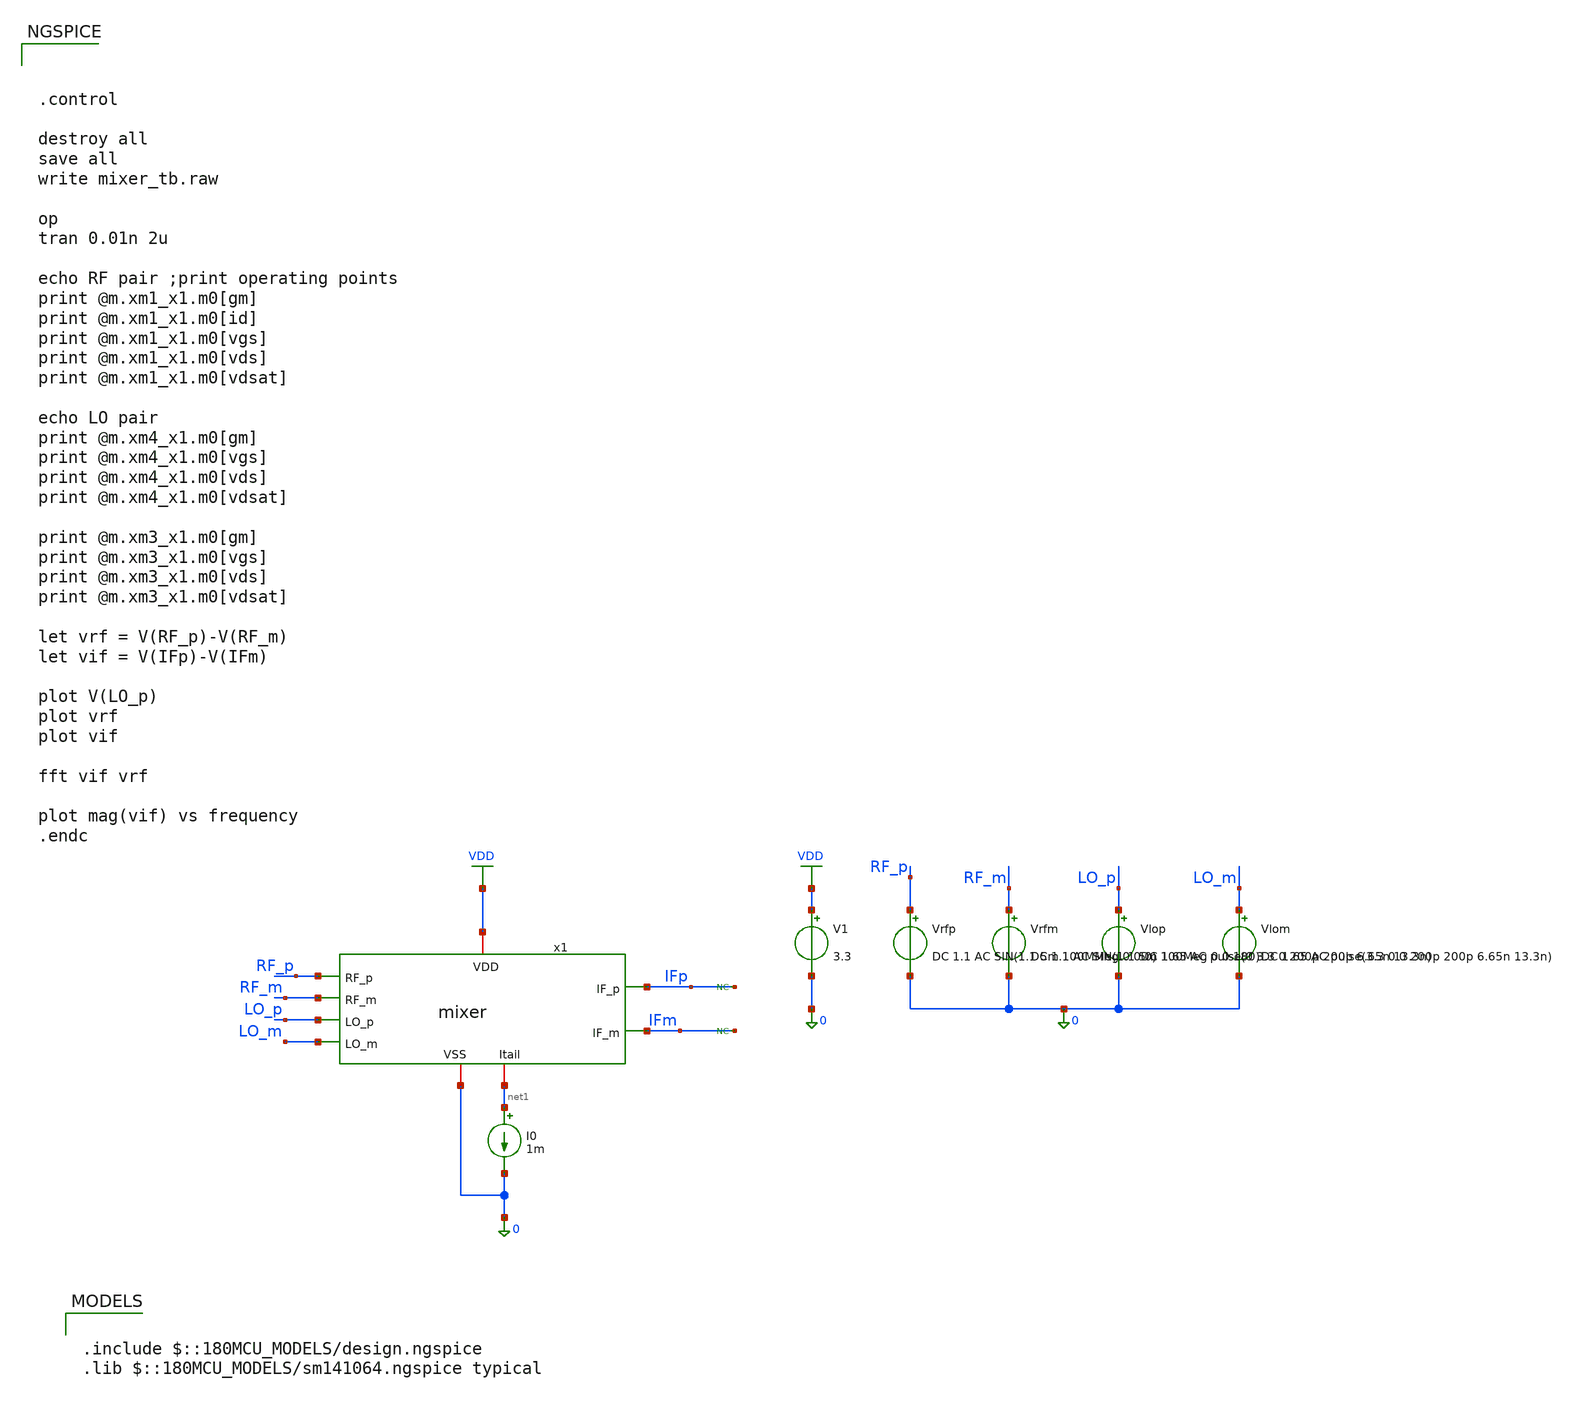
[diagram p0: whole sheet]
** sch_path: designs/mixer/testbench/mixer_tb.sch
**.subckt mixer_tb
V1 VDD 0 3.3
Vrfp RF_p 0 DC 1.1 AC SIN(1.1 5m 100MMeg 0 0 0)
Vrfm RF_m 0 DC 1.1 AC SIN(1.1 5m 100Meg 0 0 180)
I0 net1 0 1m
Vlop LO_p 0 DC 1.65 AC pulse(0 3.3 0 200p 200p 6.65n 13.3n)
Vlom LO_m 0 DC 1.65 AC pulse(3.3 0 0 200p 200p 6.65n 13.3n)
* noconn IFp
* noconn IFm
x1 IFp RF_p VDD 0 IFm RF_m LO_p net1 LO_m mixer
**** begin user architecture code

.include $::180MCU_MODELS/design.ngspice
.lib $::180MCU_MODELS/sm141064.ngspice typical




.control

destroy all
save all
write mixer_tb.raw

op
tran 0.01n 2u

echo RF pair ;print operating points
print @m.xm1_x1.m0[gm]
print @m.xm1_x1.m0[id]
print @m.xm1_x1.m0[vgs]
print @m.xm1_x1.m0[vds]
print @m.xm1_x1.m0[vdsat]

echo LO pair
print @m.xm4_x1.m0[gm]
print @m.xm4_x1.m0[vgs]
print @m.xm4_x1.m0[vds]
print @m.xm4_x1.m0[vdsat]

print @m.xm3_x1.m0[gm]
print @m.xm3_x1.m0[vgs]
print @m.xm3_x1.m0[vds]
print @m.xm3_x1.m0[vdsat]

let vrf = V(RF_p)-V(RF_m)
let vif = V(IFp)-V(IFm)

plot V(LO_p)
plot vrf
plot vif

fft vif vrf

plot mag(vif) vs frequency
.endc


**** end user architecture code
**.ends

* expanding   symbol:  /foss/designs/NYCMOS/designs/mixer/schematic/mixer.sym # of pins=9
** sym_path: designs/mixer/schematic/mixer.sym
** sch_path: designs/mixer/schematic/mixer.sch
.subckt mixer IF_p RF_p VDD VSS IF_m RF_m LO_p Itail LO_m
*.iopin VDD
*.ipin LO_p
*.ipin LO_m
*.iopin Itail
*.opin IF_m
*.opin IF_p
*.iopin VSS
*.ipin RF_p
*.ipin RF_m
XM1 net1 RF_p Itail VSS nfet_03v3 L=0.28u W=36u nf=6 ad='int((nf+1)/2) * W/nf * 0.18u' as='int((nf+2)/2) * W/nf * 0.18u'
+ pd='2*int((nf+1)/2) * (W/nf + 0.18u)' ps='2*int((nf+2)/2) * (W/nf + 0.18u)' nrd='0.18u / W' nrs='0.18u / W'
+ sa=0 sb=0 sd=0 m=1
XM2 net2 RF_m Itail VSS nfet_03v3 L=0.28u W=36u nf=6 ad='int((nf+1)/2) * W/nf * 0.18u' as='int((nf+2)/2) * W/nf * 0.18u'
+ pd='2*int((nf+1)/2) * (W/nf + 0.18u)' ps='2*int((nf+2)/2) * (W/nf + 0.18u)' nrd='0.18u / W' nrs='0.18u / W'
+ sa=0 sb=0 sd=0 m=1
XM3 IF_m LO_p net1 VSS nfet_03v3 L=0.28u W=21u nf=7 ad='int((nf+1)/2) * W/nf * 0.18u' as='int((nf+2)/2) * W/nf * 0.18u'
+ pd='2*int((nf+1)/2) * (W/nf + 0.18u)' ps='2*int((nf+2)/2) * (W/nf + 0.18u)' nrd='0.18u / W' nrs='0.18u / W'
+ sa=0 sb=0 sd=0 m=1
XM4 IF_p LO_m net1 VSS nfet_03v3 L=0.28u W=21u nf=7 ad='int((nf+1)/2) * W/nf * 0.18u' as='int((nf+2)/2) * W/nf * 0.18u'
+ pd='2*int((nf+1)/2) * (W/nf + 0.18u)' ps='2*int((nf+2)/2) * (W/nf + 0.18u)' nrd='0.18u / W' nrs='0.18u / W'
+ sa=0 sb=0 sd=0 m=1
XM5 IF_m LO_m net2 VSS nfet_03v3 L=0.28u W=21u nf=7 ad='int((nf+1)/2) * W/nf * 0.18u' as='int((nf+2)/2) * W/nf * 0.18u'
+ pd='2*int((nf+1)/2) * (W/nf + 0.18u)' ps='2*int((nf+2)/2) * (W/nf + 0.18u)' nrd='0.18u / W' nrs='0.18u / W'
+ sa=0 sb=0 sd=0 m=1
XM6 IF_p LO_p net2 VSS nfet_03v3 L=0.28u W=21u nf=7 ad='int((nf+1)/2) * W/nf * 0.18u' as='int((nf+2)/2) * W/nf * 0.18u'
+ pd='2*int((nf+1)/2) * (W/nf + 0.18u)' ps='2*int((nf+2)/2) * (W/nf + 0.18u)' nrd='0.18u / W' nrs='0.18u / W'
+ sa=0 sb=0 sd=0 m=1
XR1 IF_m VDD VSS ppolyf_u_1k r_width=1e-6 r_length=1.8e-6 m=1
XR2 IF_p VDD VSS ppolyf_u_1k r_width=1e-6 r_length=1.8e-6 m=1
.ends

.GLOBAL VDD
.end
